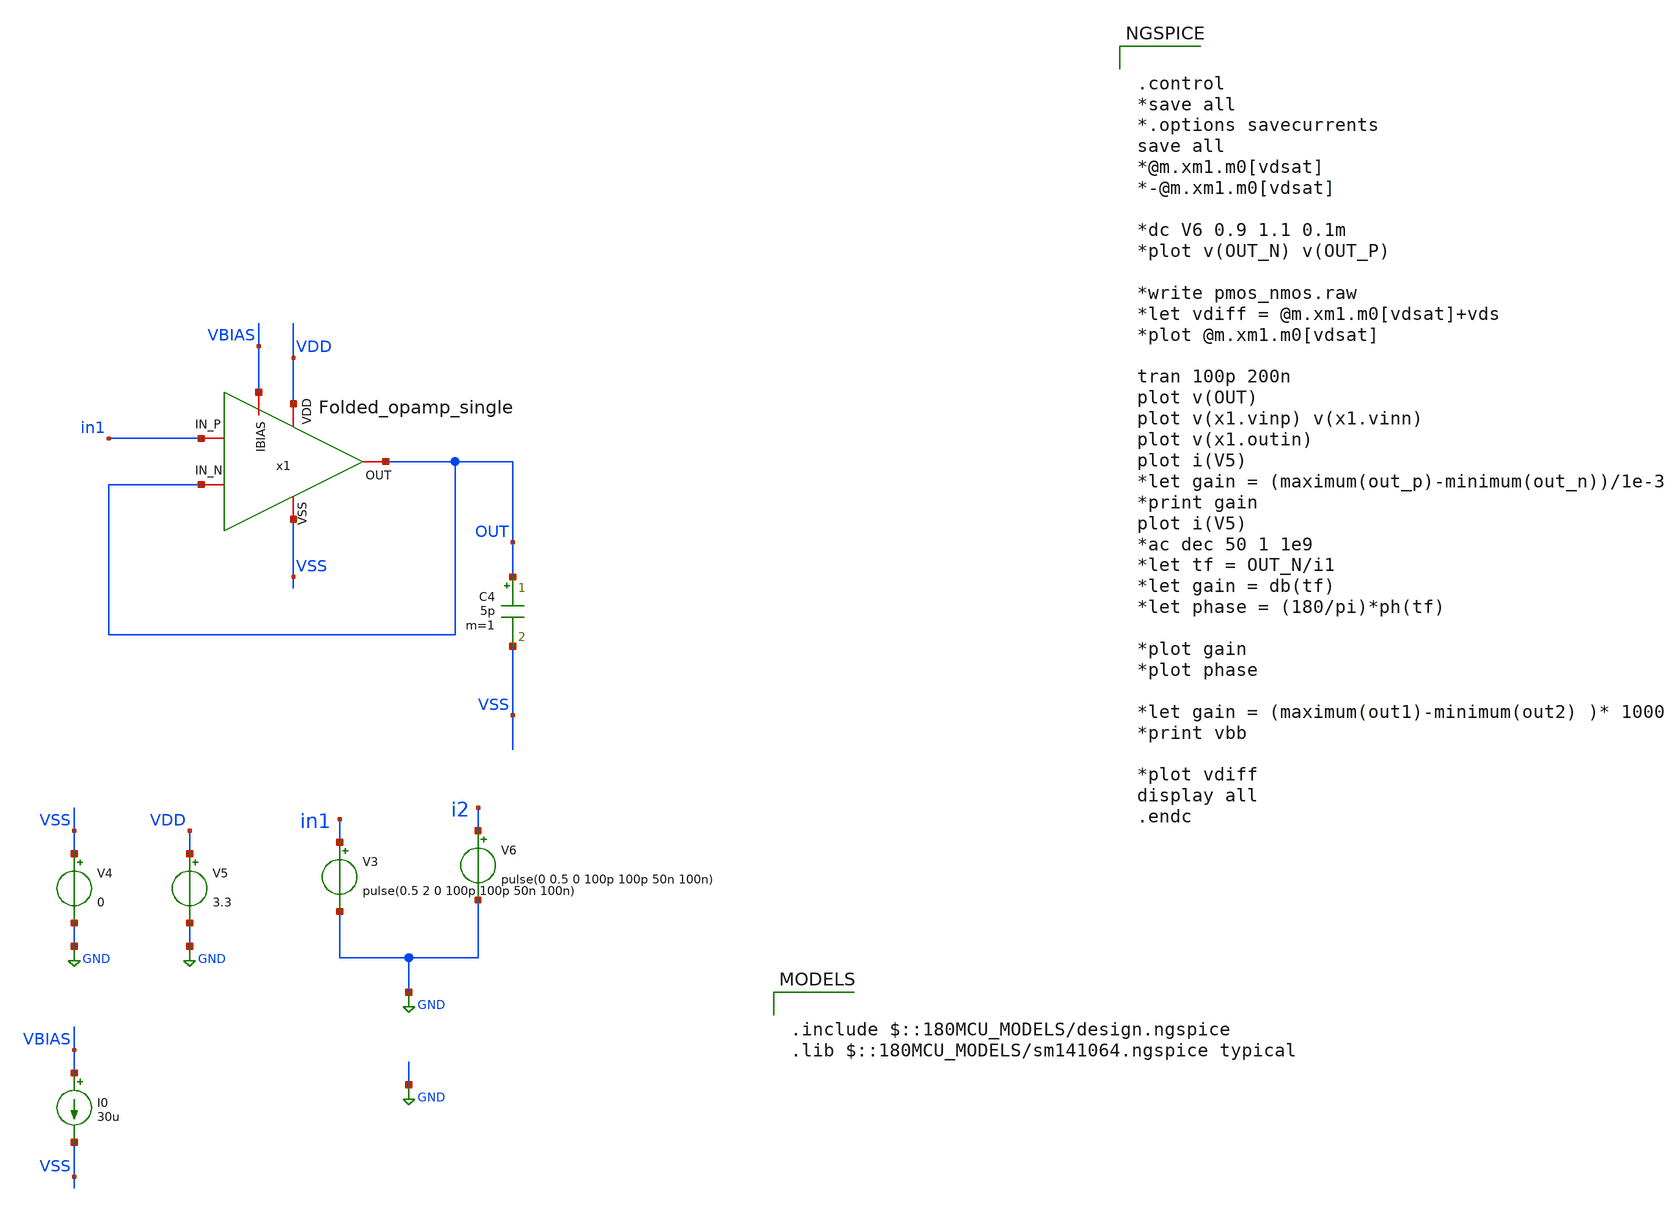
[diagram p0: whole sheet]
** sch_path: SCOP_INPUT_AND_MUX_PAKISTAN_03/Xschem/Folded_single/OTA_two_stage_slew.sch
**.subckt OTA_two_stage_slew
V3 in1 GND pulse(0.5 2 0 100p 100p 50n 100n)
V4 VSS GND 0
V5 VDD GND 3.3
V6 i2 GND pulse(0 0.5 0 100p 100p 50n 100n)
C4 OUT VSS 5p m=1
I0 VBIAS VSS 30u
x1 OUT VDD VSS OUT in1 VBIAS Folded_opamp_single
**** begin user architecture code

.include $::180MCU_MODELS/design.ngspice
.lib $::180MCU_MODELS/sm141064.ngspice typical



.control
*save all
*.options savecurrents
save all
*@m.xm1.m0[vdsat]
*-@m.xm1.m0[vdsat]

*dc V6 0.9 1.1 0.1m
*plot v(OUT_N) v(OUT_P)

*write pmos_nmos.raw
*let vdiff = @m.xm1.m0[vdsat]+vds
*plot @m.xm1.m0[vdsat]

tran 100p 200n
plot v(OUT)
plot v(x1.vinp) v(x1.vinn)
plot v(x1.outin)
plot i(V5)
*let gain = (maximum(out_p)-minimum(out_n))/1e-3
*print gain
plot i(V5)
*ac dec 50 1 1e9
*let tf = OUT_N/i1
*let gain = db(tf)
*let phase = (180/pi)*ph(tf)

*plot gain
*plot phase

*let gain = (maximum(out1)-minimum(out2) )* 1000
*print vbb

*plot vdiff
display all
.endc


**** end user architecture code
**.ends
.GLOBAL GND
.end
